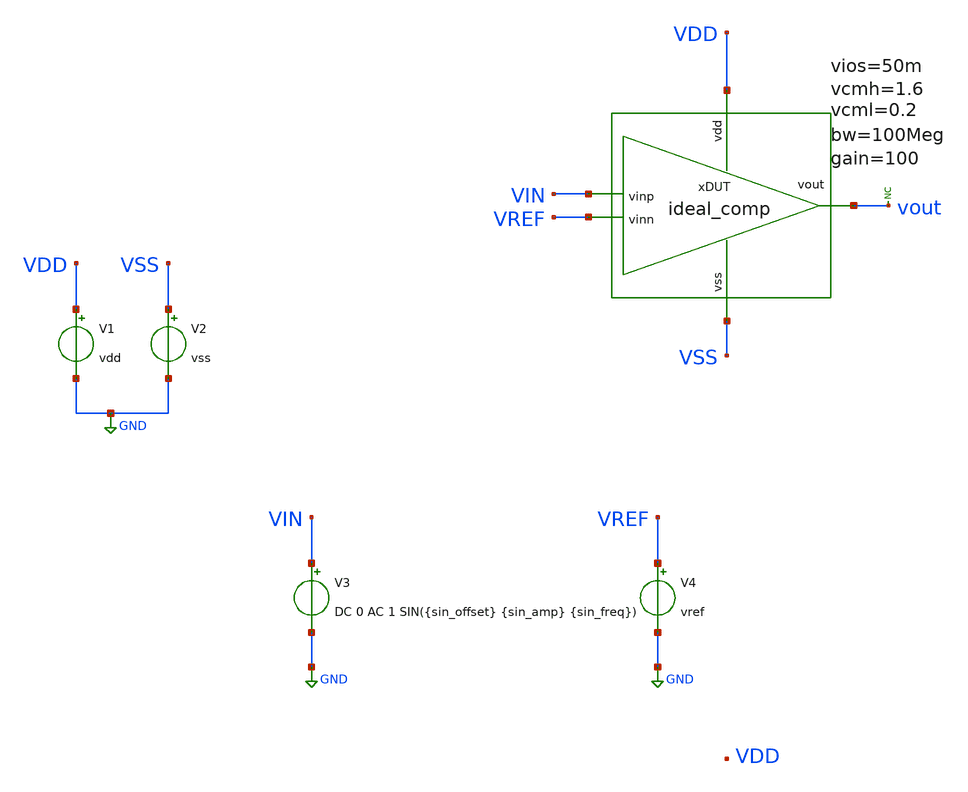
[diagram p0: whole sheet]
** sch_path: simulation/tb_comp_top.sch
**.subckt tb_comp_top
V1 VDD GND vdd
V2 VSS GND vss
V3 VIN GND DC 0 AC 1 SIN({sin_offset} {sin_amp} {sin_freq})
V4 VREF GND vref
xDUT VDD VSS VIN vout VREF ideal_comp bw=100Meg gain=100 vdd= vss= vin_h= vin_l= vios=50m
* noconn vout
**** begin user architecture code



# Model files
.lib /usr/local/share/pdk/sky130A/libs.tech/ngspice/sky130.lib.spice tt

# Main parameters
.param vdd=1.8 vss=0 vref='vdd/2' vhigh=1.8 vlow=0
.param sin_offset='vdd/2'
.param sin_amp='vdd/2'
.param sin_freq=10Meg
.param sin_period='1/sin_freq'
.param tran_step='sin_period/10'
.param tran_stop_time='sin_period*2'

# Component parameters



# Save settings
.save all


# Analysis
.op
.tran {tran_step} {tran_stop_time}

# Start control block
.control

# Run sim
run

# Expressions

# Save expressions

# Write to raw file
write tb_comp_top.raw
# wrdata custom_output.txt



.endc



**** end user architecture code
**.ends

* expanding   symbol:  schematics/ideal_comp.sym # of pins=5
** sym_path: schematics/ideal_comp.sym
** sch_path: schematics/ideal_comp.sch
.subckt ideal_comp vdd vss vinp vout vinn  bw=100Meg gain=100 vcmh=1.6 vcml=0.2 vios=50m
*.ipin vdd
*.opin vout
*.ipin vss
*.ipin vinp
*.ipin vinn
E1 vcvs_out vss vinp vinn 1e6
B1 vout vss v=( V(vcvs_out) < {vlow} ? {vlow} : (V(vcvs_out) > {vhigh} ? {vhigh} : V(vcvs_out)))
.ends

.GLOBAL GND
.end
